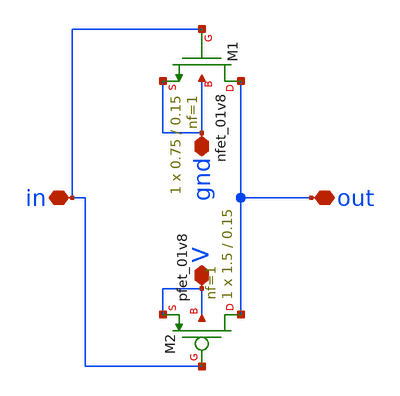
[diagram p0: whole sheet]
** sch_path: xschem/designs/counter4b/inv_gate.sch
**.subckt inv_gate in out gnd V
*.iopin in
*.iopin out
*.iopin gnd
*.iopin V
XM1 out in gnd gnd sky130_fd_pr__nfet_01v8 L=0.15 W=0.75 nf=1 ad='int((nf+1)/2) * W/nf * 0.29' as='int((nf+2)/2) * W/nf * 0.29'
+ pd='2*int((nf+1)/2) * (W/nf + 0.29)' ps='2*int((nf+2)/2) * (W/nf + 0.29)' nrd='0.29 / W' nrs='0.29 / W'
+ sa=0 sb=0 sd=0 mult=1 m=1
XM2 out in V V sky130_fd_pr__pfet_01v8 L=0.15 W=1.5 nf=1 ad='int((nf+1)/2) * W/nf * 0.29' as='int((nf+2)/2) * W/nf * 0.29'
+ pd='2*int((nf+1)/2) * (W/nf + 0.29)' ps='2*int((nf+2)/2) * (W/nf + 0.29)' nrd='0.29 / W' nrs='0.29 / W'
+ sa=0 sb=0 sd=0 mult=1 m=1
**.ends
.end
